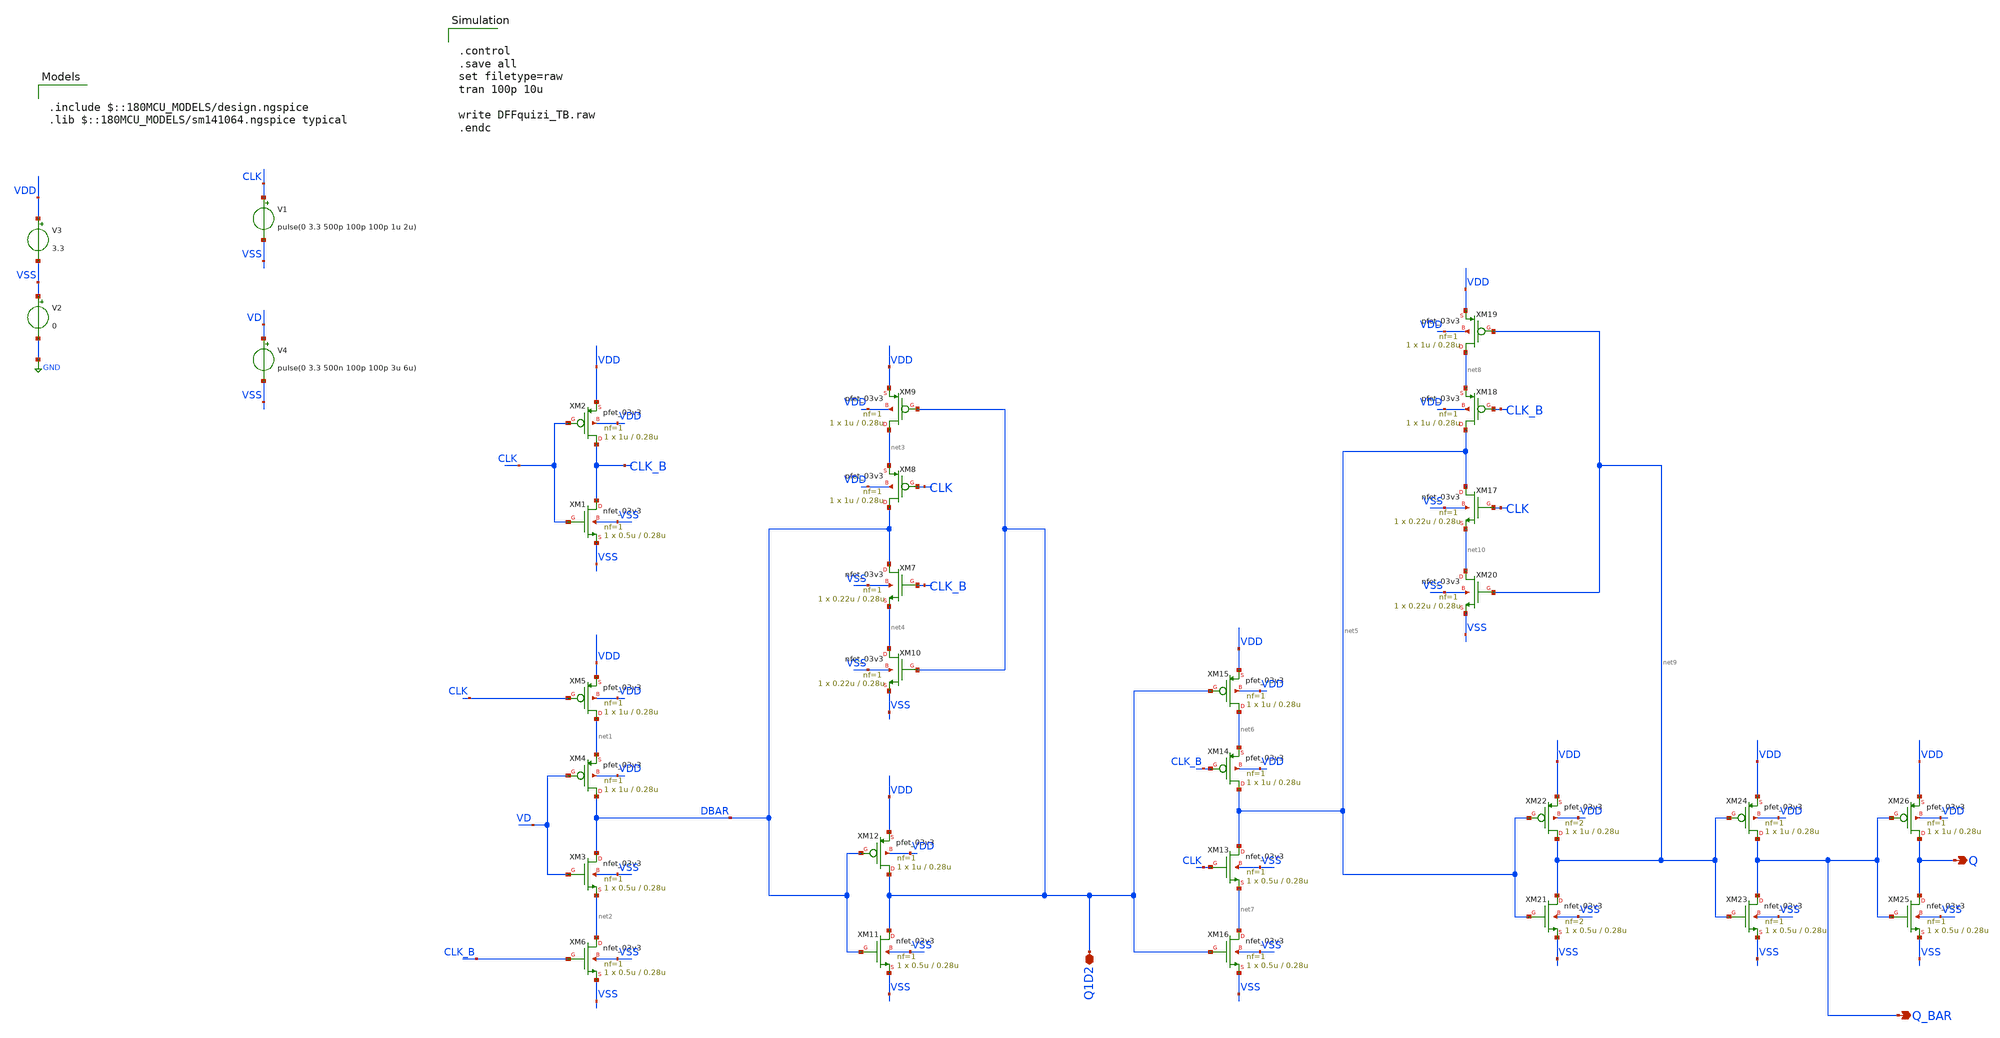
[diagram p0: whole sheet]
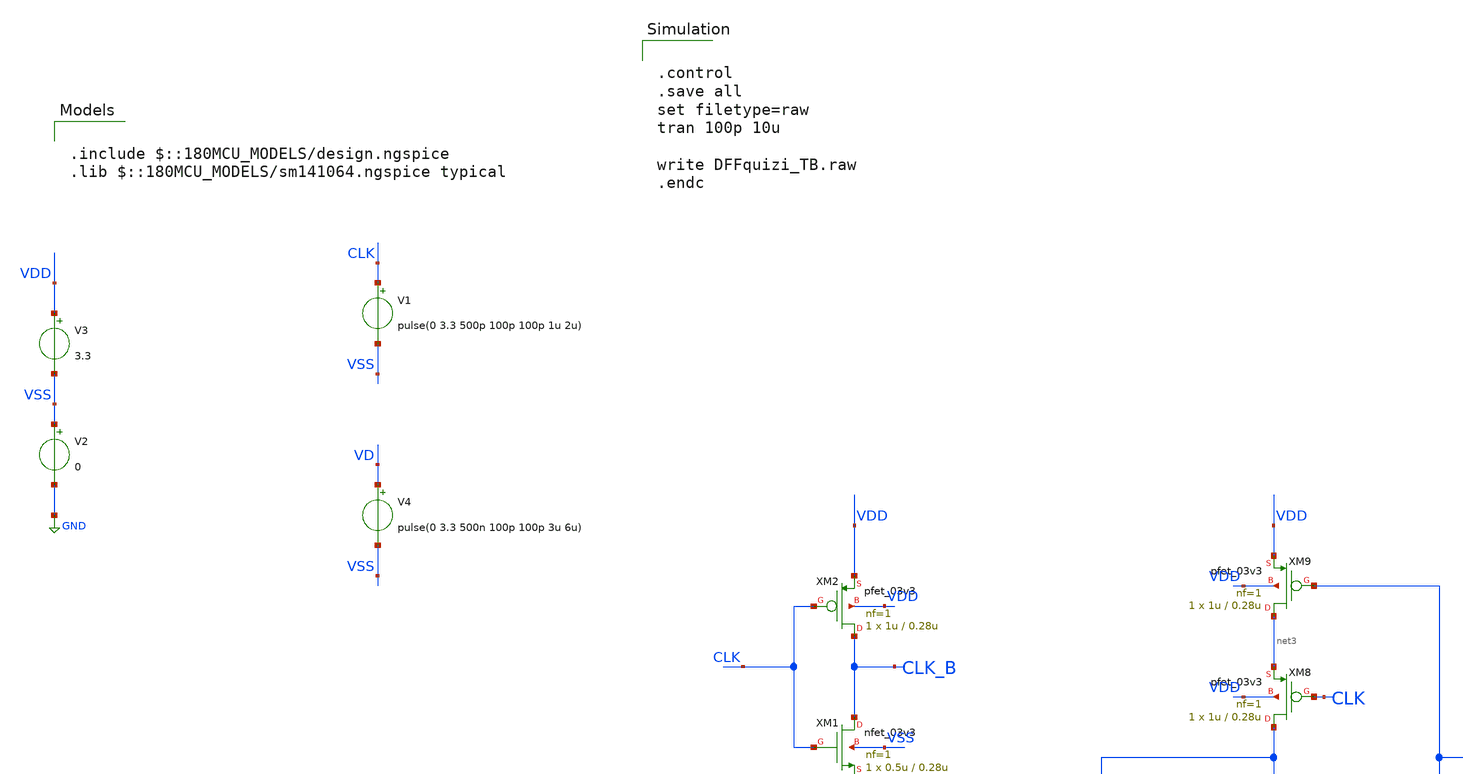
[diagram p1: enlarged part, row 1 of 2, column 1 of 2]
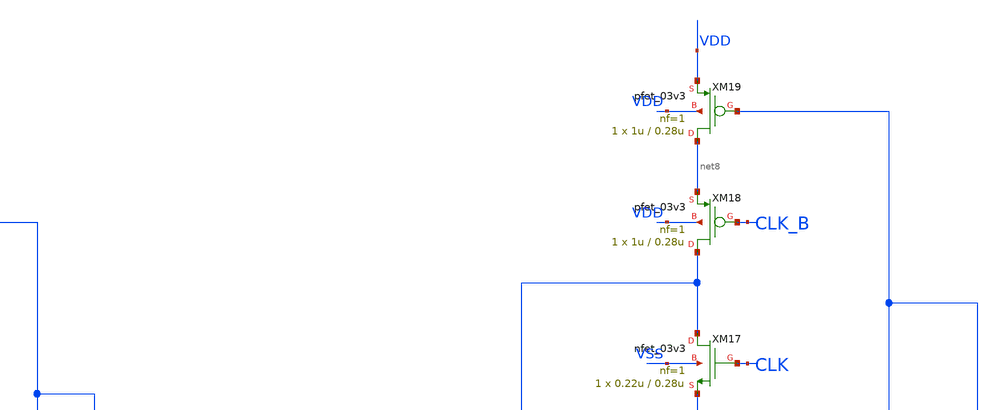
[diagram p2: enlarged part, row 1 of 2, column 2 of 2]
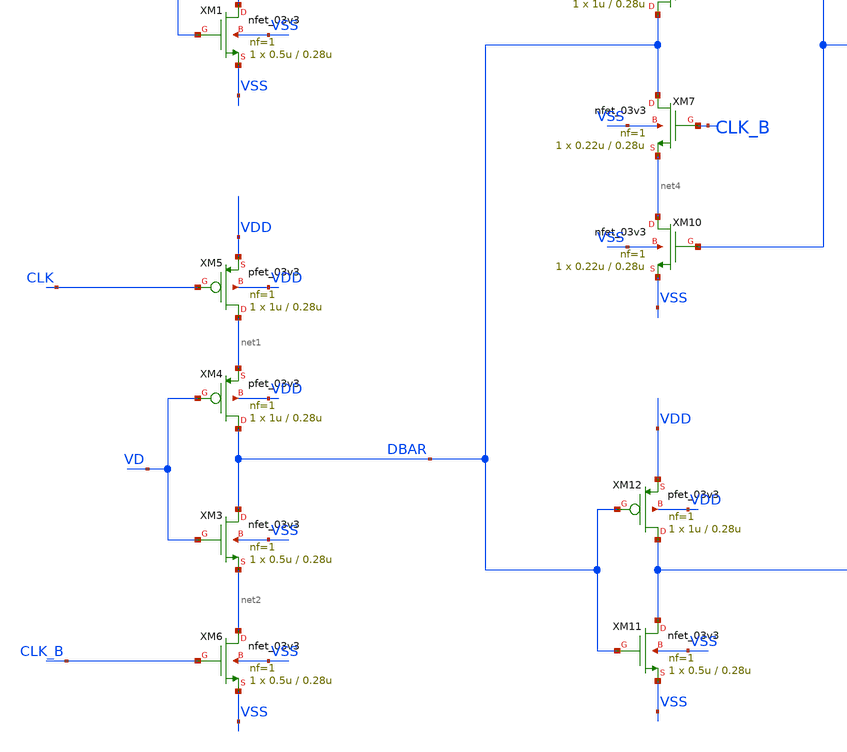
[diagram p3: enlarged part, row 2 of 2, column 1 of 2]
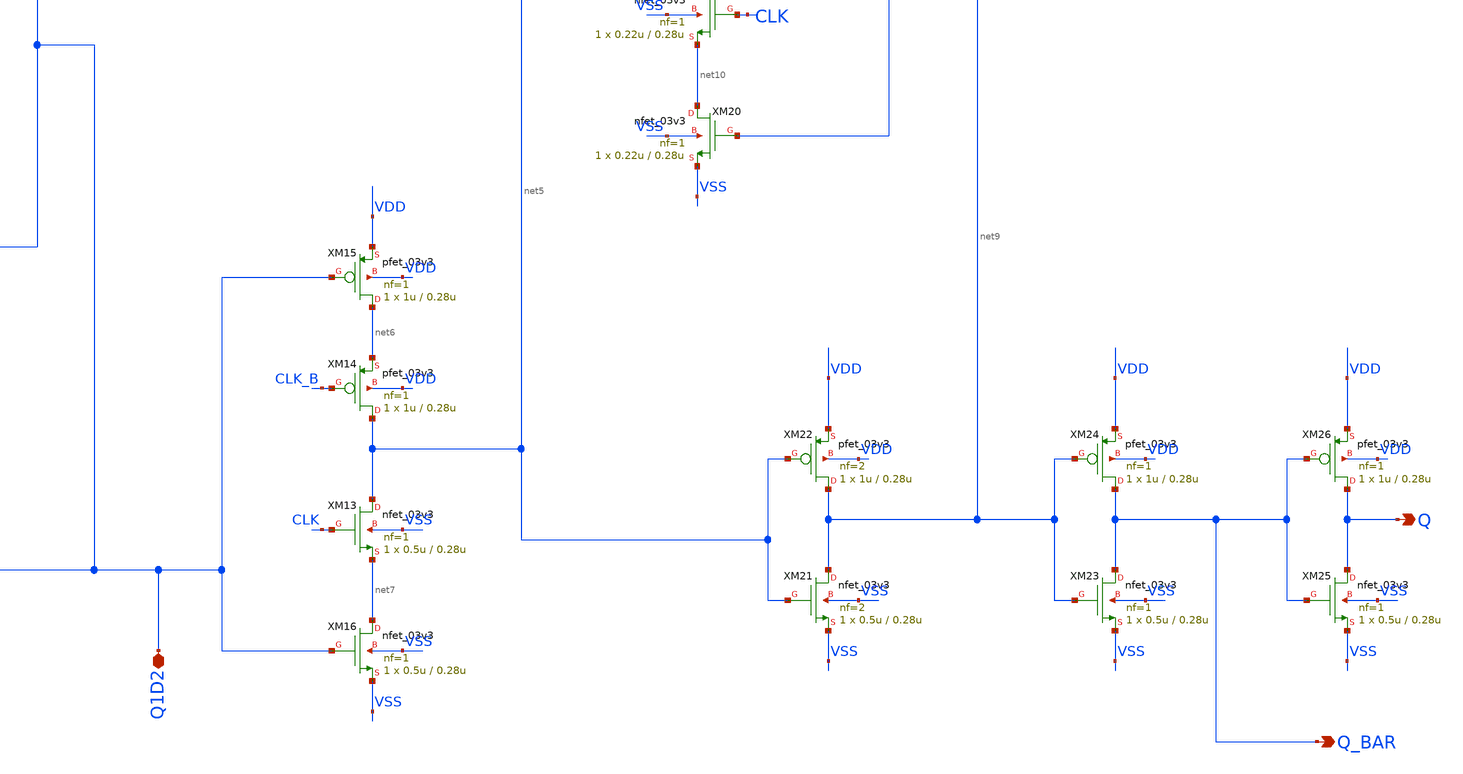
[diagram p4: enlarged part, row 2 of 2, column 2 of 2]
** sch_path: designs/libs/qw_core_analog/DFFquizi_TB.sch
**.subckt DFFquizi_TB Q_BAR Q Q1D2
*.opin Q_BAR
*.opin Q
*.iopin Q1D2
V1 CLK VSS pulse(0 3.3 500p 100p 100p 1u 2u)
V2 VSS GND 0
V3 VDD VSS 3.3
V4 VD VSS pulse(0 3.3 500n 100p 100p 3u 6u)
XM1 CLK_B CLK VSS VSS nfet_03v3 L=0.28u W=0.5u nf=1 ad='int((nf+1)/2) * W/nf * 0.18u' as='int((nf+2)/2) * W/nf * 0.18u'
+ pd='2*int((nf+1)/2) * (W/nf + 0.18u)' ps='2*int((nf+2)/2) * (W/nf + 0.18u)' nrd='0.18u / W' nrs='0.18u / W'
+ sa=0 sb=0 sd=0 m=1
XM2 CLK_B CLK VDD VDD pfet_03v3 L=0.28u W=1u nf=1 ad='int((nf+1)/2) * W/nf * 0.18u' as='int((nf+2)/2) * W/nf * 0.18u'
+ pd='2*int((nf+1)/2) * (W/nf + 0.18u)' ps='2*int((nf+2)/2) * (W/nf + 0.18u)' nrd='0.18u / W' nrs='0.18u / W'
+ sa=0 sb=0 sd=0 m=1
XM3 DBAR VD net2 VSS nfet_03v3 L=0.28u W=0.5u nf=1 ad='int((nf+1)/2) * W/nf * 0.18u' as='int((nf+2)/2) * W/nf * 0.18u'
+ pd='2*int((nf+1)/2) * (W/nf + 0.18u)' ps='2*int((nf+2)/2) * (W/nf + 0.18u)' nrd='0.18u / W' nrs='0.18u / W'
+ sa=0 sb=0 sd=0 m=1
XM4 DBAR VD net1 VDD pfet_03v3 L=0.28u W=1u nf=1 ad='int((nf+1)/2) * W/nf * 0.18u' as='int((nf+2)/2) * W/nf * 0.18u'
+ pd='2*int((nf+1)/2) * (W/nf + 0.18u)' ps='2*int((nf+2)/2) * (W/nf + 0.18u)' nrd='0.18u / W' nrs='0.18u / W'
+ sa=0 sb=0 sd=0 m=1
XM5 net1 CLK VDD VDD pfet_03v3 L=0.28u W=1u nf=1 ad='int((nf+1)/2) * W/nf * 0.18u' as='int((nf+2)/2) * W/nf * 0.18u'
+ pd='2*int((nf+1)/2) * (W/nf + 0.18u)' ps='2*int((nf+2)/2) * (W/nf + 0.18u)' nrd='0.18u / W' nrs='0.18u / W'
+ sa=0 sb=0 sd=0 m=1
XM6 net2 CLK_B VSS VSS nfet_03v3 L=0.28u W=0.5u nf=1 ad='int((nf+1)/2) * W/nf * 0.18u' as='int((nf+2)/2) * W/nf * 0.18u'
+ pd='2*int((nf+1)/2) * (W/nf + 0.18u)' ps='2*int((nf+2)/2) * (W/nf + 0.18u)' nrd='0.18u / W' nrs='0.18u / W'
+ sa=0 sb=0 sd=0 m=1
XM7 DBAR CLK_B net4 VSS nfet_03v3 L=0.28u W=0.22u nf=1 ad='int((nf+1)/2) * W/nf * 0.18u' as='int((nf+2)/2) * W/nf * 0.18u'
+ pd='2*int((nf+1)/2) * (W/nf + 0.18u)' ps='2*int((nf+2)/2) * (W/nf + 0.18u)' nrd='0.18u / W' nrs='0.18u / W'
+ sa=0 sb=0 sd=0 m=1
XM8 DBAR CLK net3 VDD pfet_03v3 L=0.28u W=1u nf=1 ad='int((nf+1)/2) * W/nf * 0.18u' as='int((nf+2)/2) * W/nf * 0.18u'
+ pd='2*int((nf+1)/2) * (W/nf + 0.18u)' ps='2*int((nf+2)/2) * (W/nf + 0.18u)' nrd='0.18u / W' nrs='0.18u / W'
+ sa=0 sb=0 sd=0 m=1
XM9 net3 Q1D2 VDD VDD pfet_03v3 L=0.28u W=1u nf=1 ad='int((nf+1)/2) * W/nf * 0.18u' as='int((nf+2)/2) * W/nf * 0.18u'
+ pd='2*int((nf+1)/2) * (W/nf + 0.18u)' ps='2*int((nf+2)/2) * (W/nf + 0.18u)' nrd='0.18u / W' nrs='0.18u / W'
+ sa=0 sb=0 sd=0 m=1
XM10 net4 Q1D2 VSS VSS nfet_03v3 L=0.28u W=0.22u nf=1 ad='int((nf+1)/2) * W/nf * 0.18u' as='int((nf+2)/2) * W/nf * 0.18u'
+ pd='2*int((nf+1)/2) * (W/nf + 0.18u)' ps='2*int((nf+2)/2) * (W/nf + 0.18u)' nrd='0.18u / W' nrs='0.18u / W'
+ sa=0 sb=0 sd=0 m=1
XM11 Q1D2 DBAR VSS VSS nfet_03v3 L=0.28u W=0.5u nf=1 ad='int((nf+1)/2) * W/nf * 0.18u' as='int((nf+2)/2) * W/nf * 0.18u'
+ pd='2*int((nf+1)/2) * (W/nf + 0.18u)' ps='2*int((nf+2)/2) * (W/nf + 0.18u)' nrd='0.18u / W' nrs='0.18u / W'
+ sa=0 sb=0 sd=0 m=1
XM12 Q1D2 DBAR VDD VDD pfet_03v3 L=0.28u W=1u nf=1 ad='int((nf+1)/2) * W/nf * 0.18u' as='int((nf+2)/2) * W/nf * 0.18u'
+ pd='2*int((nf+1)/2) * (W/nf + 0.18u)' ps='2*int((nf+2)/2) * (W/nf + 0.18u)' nrd='0.18u / W' nrs='0.18u / W'
+ sa=0 sb=0 sd=0 m=1
XM13 net5 CLK net7 VSS nfet_03v3 L=0.28u W=0.5u nf=1 ad='int((nf+1)/2) * W/nf * 0.18u' as='int((nf+2)/2) * W/nf * 0.18u'
+ pd='2*int((nf+1)/2) * (W/nf + 0.18u)' ps='2*int((nf+2)/2) * (W/nf + 0.18u)' nrd='0.18u / W' nrs='0.18u / W'
+ sa=0 sb=0 sd=0 m=1
XM14 net5 CLK_B net6 VDD pfet_03v3 L=0.28u W=1u nf=1 ad='int((nf+1)/2) * W/nf * 0.18u' as='int((nf+2)/2) * W/nf * 0.18u'
+ pd='2*int((nf+1)/2) * (W/nf + 0.18u)' ps='2*int((nf+2)/2) * (W/nf + 0.18u)' nrd='0.18u / W' nrs='0.18u / W'
+ sa=0 sb=0 sd=0 m=1
XM15 net6 Q1D2 VDD VDD pfet_03v3 L=0.28u W=1u nf=1 ad='int((nf+1)/2) * W/nf * 0.18u' as='int((nf+2)/2) * W/nf * 0.18u'
+ pd='2*int((nf+1)/2) * (W/nf + 0.18u)' ps='2*int((nf+2)/2) * (W/nf + 0.18u)' nrd='0.18u / W' nrs='0.18u / W'
+ sa=0 sb=0 sd=0 m=1
XM16 net7 Q1D2 VSS VSS nfet_03v3 L=0.28u W=0.5u nf=1 ad='int((nf+1)/2) * W/nf * 0.18u' as='int((nf+2)/2) * W/nf * 0.18u'
+ pd='2*int((nf+1)/2) * (W/nf + 0.18u)' ps='2*int((nf+2)/2) * (W/nf + 0.18u)' nrd='0.18u / W' nrs='0.18u / W'
+ sa=0 sb=0 sd=0 m=1
XM17 net5 CLK net10 VSS nfet_03v3 L=0.28u W=0.22u nf=1 ad='int((nf+1)/2) * W/nf * 0.18u' as='int((nf+2)/2) * W/nf * 0.18u'
+ pd='2*int((nf+1)/2) * (W/nf + 0.18u)' ps='2*int((nf+2)/2) * (W/nf + 0.18u)' nrd='0.18u / W' nrs='0.18u / W'
+ sa=0 sb=0 sd=0 m=1
XM18 net5 CLK_B net8 VDD pfet_03v3 L=0.28u W=1u nf=1 ad='int((nf+1)/2) * W/nf * 0.18u' as='int((nf+2)/2) * W/nf * 0.18u'
+ pd='2*int((nf+1)/2) * (W/nf + 0.18u)' ps='2*int((nf+2)/2) * (W/nf + 0.18u)' nrd='0.18u / W' nrs='0.18u / W'
+ sa=0 sb=0 sd=0 m=1
XM19 net8 net9 VDD VDD pfet_03v3 L=0.28u W=1u nf=1 ad='int((nf+1)/2) * W/nf * 0.18u' as='int((nf+2)/2) * W/nf * 0.18u'
+ pd='2*int((nf+1)/2) * (W/nf + 0.18u)' ps='2*int((nf+2)/2) * (W/nf + 0.18u)' nrd='0.18u / W' nrs='0.18u / W'
+ sa=0 sb=0 sd=0 m=1
XM20 net10 net9 VSS VSS nfet_03v3 L=0.28u W=0.22u nf=1 ad='int((nf+1)/2) * W/nf * 0.18u' as='int((nf+2)/2) * W/nf * 0.18u'
+ pd='2*int((nf+1)/2) * (W/nf + 0.18u)' ps='2*int((nf+2)/2) * (W/nf + 0.18u)' nrd='0.18u / W' nrs='0.18u / W'
+ sa=0 sb=0 sd=0 m=1
XM21 net9 net5 VSS VSS nfet_03v3 L=0.28u W=0.5u nf=2 ad='int((nf+1)/2) * W/nf * 0.18u' as='int((nf+2)/2) * W/nf * 0.18u'
+ pd='2*int((nf+1)/2) * (W/nf + 0.18u)' ps='2*int((nf+2)/2) * (W/nf + 0.18u)' nrd='0.18u / W' nrs='0.18u / W'
+ sa=0 sb=0 sd=0 m=1
XM22 net9 net5 VDD VDD pfet_03v3 L=0.28u W=1u nf=2 ad='int((nf+1)/2) * W/nf * 0.18u' as='int((nf+2)/2) * W/nf * 0.18u'
+ pd='2*int((nf+1)/2) * (W/nf + 0.18u)' ps='2*int((nf+2)/2) * (W/nf + 0.18u)' nrd='0.18u / W' nrs='0.18u / W'
+ sa=0 sb=0 sd=0 m=1
XM23 Q_BAR net9 VSS VSS nfet_03v3 L=0.28u W=0.5u nf=1 ad='int((nf+1)/2) * W/nf * 0.18u' as='int((nf+2)/2) * W/nf * 0.18u'
+ pd='2*int((nf+1)/2) * (W/nf + 0.18u)' ps='2*int((nf+2)/2) * (W/nf + 0.18u)' nrd='0.18u / W' nrs='0.18u / W'
+ sa=0 sb=0 sd=0 m=1
XM24 Q_BAR net9 VDD VDD pfet_03v3 L=0.28u W=1u nf=1 ad='int((nf+1)/2) * W/nf * 0.18u' as='int((nf+2)/2) * W/nf * 0.18u'
+ pd='2*int((nf+1)/2) * (W/nf + 0.18u)' ps='2*int((nf+2)/2) * (W/nf + 0.18u)' nrd='0.18u / W' nrs='0.18u / W'
+ sa=0 sb=0 sd=0 m=1
XM25 Q Q_BAR VSS VSS nfet_03v3 L=0.28u W=0.5u nf=1 ad='int((nf+1)/2) * W/nf * 0.18u' as='int((nf+2)/2) * W/nf * 0.18u'
+ pd='2*int((nf+1)/2) * (W/nf + 0.18u)' ps='2*int((nf+2)/2) * (W/nf + 0.18u)' nrd='0.18u / W' nrs='0.18u / W'
+ sa=0 sb=0 sd=0 m=1
XM26 Q Q_BAR VDD VDD pfet_03v3 L=0.28u W=1u nf=1 ad='int((nf+1)/2) * W/nf * 0.18u' as='int((nf+2)/2) * W/nf * 0.18u'
+ pd='2*int((nf+1)/2) * (W/nf + 0.18u)' ps='2*int((nf+2)/2) * (W/nf + 0.18u)' nrd='0.18u / W' nrs='0.18u / W'
+ sa=0 sb=0 sd=0 m=1
**** begin user architecture code

.include $::180MCU_MODELS/design.ngspice
.lib $::180MCU_MODELS/sm141064.ngspice typical



.control
.save all
set filetype=raw
tran 100p 10u

write DFFquizi_TB.raw
.endc


**** end user architecture code
**.ends
.GLOBAL GND
.end
